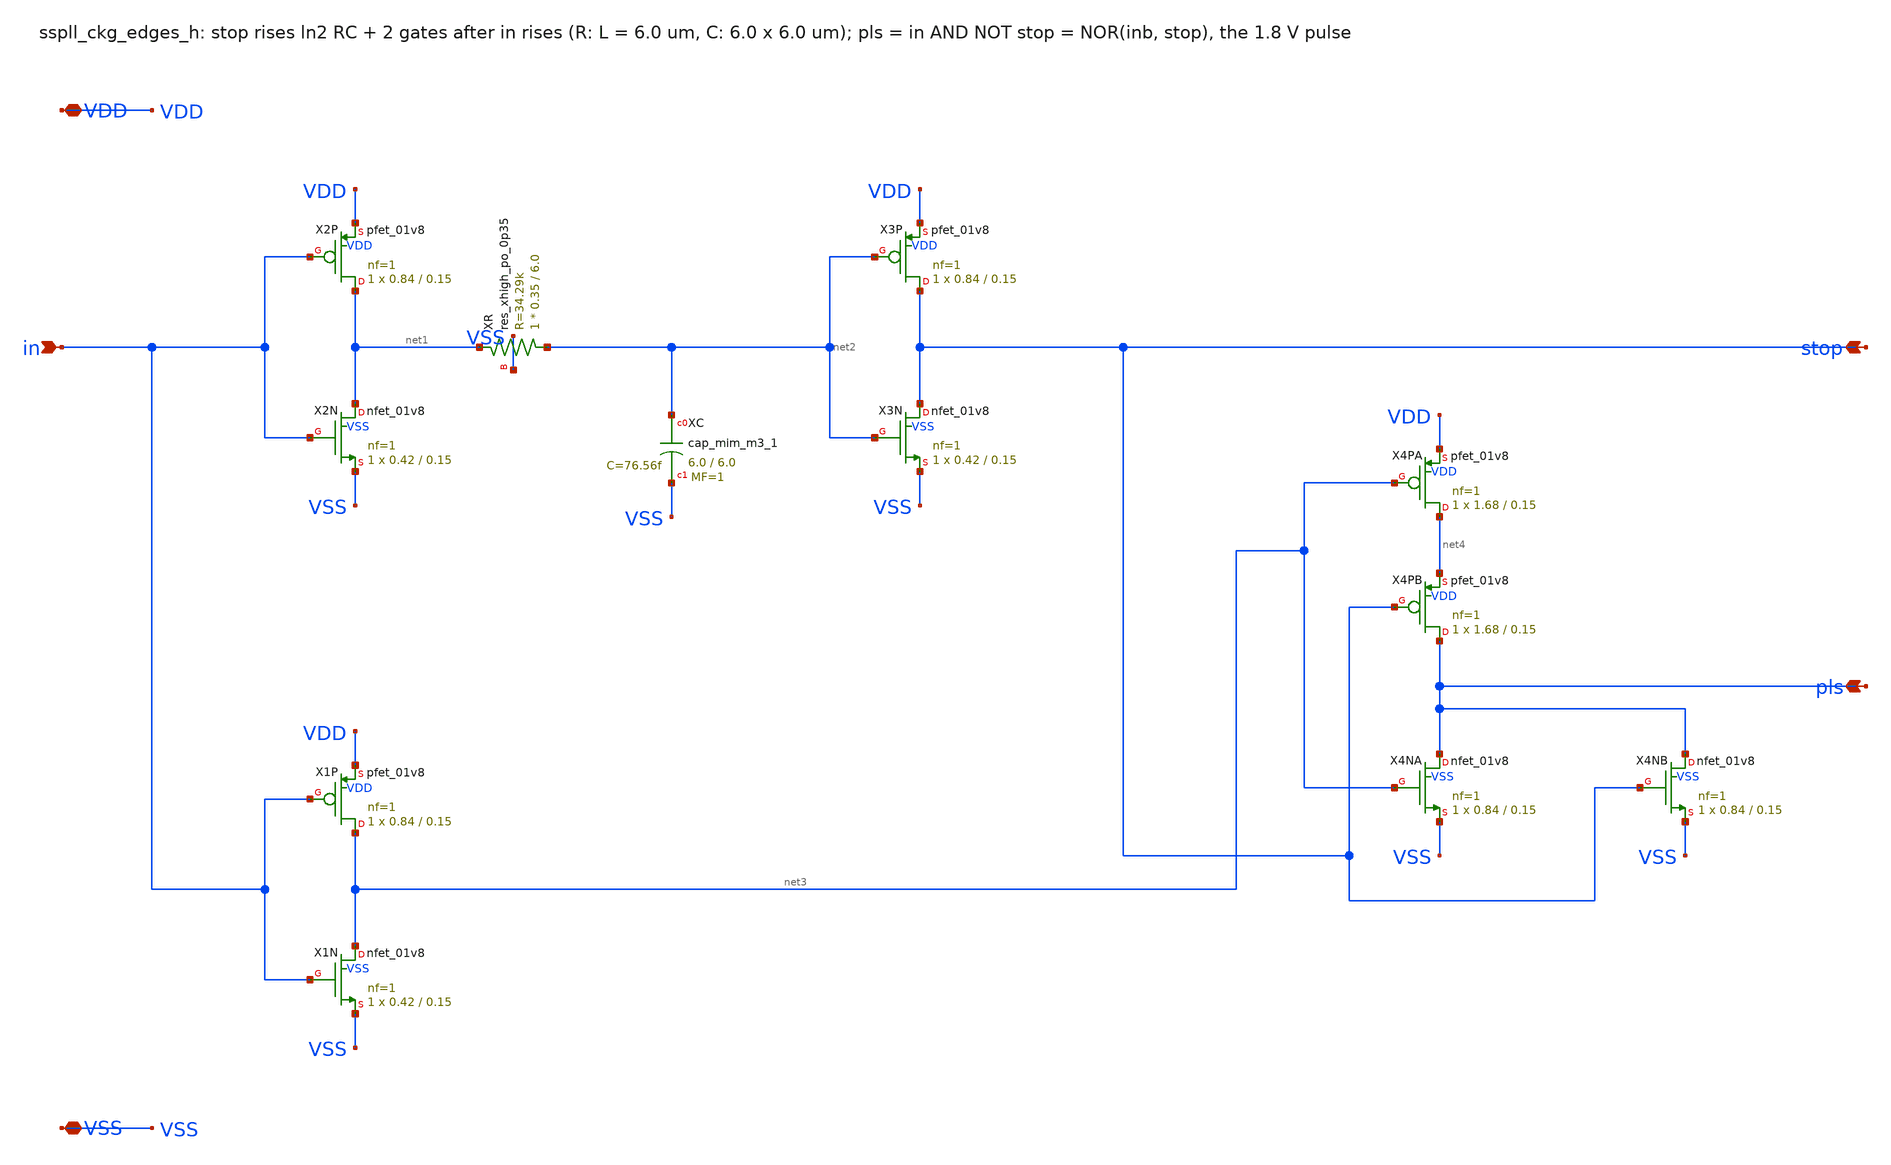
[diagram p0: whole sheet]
** sch_path: xschem/clkgen_hv/sspll_ckg_edges_h.sch
**.subckt sspll_ckg_edges_h in stop pls VDD VSS
*.ipin in
*.opin stop
*.opin pls
*.iopin VDD
*.iopin VSS
XX2P net1 in VDD VDD sky130_fd_pr__pfet_01v8 L=0.15 W=0.84 nf=1 ad='int((nf+1)/2) * W/nf * 0.29' as='int((nf+2)/2) * W/nf * 0.29'
+ pd='2*int((nf+1)/2) * (W/nf + 0.29)' ps='2*int((nf+2)/2) * (W/nf + 0.29)' nrd='0.29 / W' nrs='0.29 / W'
+ sa=0 sb=0 sd=0 mult=1 m=1
XX2N net1 in VSS VSS sky130_fd_pr__nfet_01v8 L=0.15 W=0.42 nf=1 ad='int((nf+1)/2) * W/nf * 0.29' as='int((nf+2)/2) * W/nf * 0.29'
+ pd='2*int((nf+1)/2) * (W/nf + 0.29)' ps='2*int((nf+2)/2) * (W/nf + 0.29)' nrd='0.29 / W' nrs='0.29 / W'
+ sa=0 sb=0 sd=0 mult=1 m=1
XXR net2 net1 VSS sky130_fd_pr__res_xhigh_po_0p35 L=6.0 mult=1 m=1
XXC net2 VSS sky130_fd_pr__cap_mim_m3_1 W=6.0 L=6.0 MF=1 m=1
XX3P stop net2 VDD VDD sky130_fd_pr__pfet_01v8 L=0.15 W=0.84 nf=1 ad='int((nf+1)/2) * W/nf * 0.29' as='int((nf+2)/2) * W/nf * 0.29'
+ pd='2*int((nf+1)/2) * (W/nf + 0.29)' ps='2*int((nf+2)/2) * (W/nf + 0.29)' nrd='0.29 / W' nrs='0.29 / W'
+ sa=0 sb=0 sd=0 mult=1 m=1
XX3N stop net2 VSS VSS sky130_fd_pr__nfet_01v8 L=0.15 W=0.42 nf=1 ad='int((nf+1)/2) * W/nf * 0.29' as='int((nf+2)/2) * W/nf * 0.29'
+ pd='2*int((nf+1)/2) * (W/nf + 0.29)' ps='2*int((nf+2)/2) * (W/nf + 0.29)' nrd='0.29 / W' nrs='0.29 / W'
+ sa=0 sb=0 sd=0 mult=1 m=1
XX1P net3 in VDD VDD sky130_fd_pr__pfet_01v8 L=0.15 W=0.84 nf=1 ad='int((nf+1)/2) * W/nf * 0.29' as='int((nf+2)/2) * W/nf * 0.29'
+ pd='2*int((nf+1)/2) * (W/nf + 0.29)' ps='2*int((nf+2)/2) * (W/nf + 0.29)' nrd='0.29 / W' nrs='0.29 / W'
+ sa=0 sb=0 sd=0 mult=1 m=1
XX1N net3 in VSS VSS sky130_fd_pr__nfet_01v8 L=0.15 W=0.42 nf=1 ad='int((nf+1)/2) * W/nf * 0.29' as='int((nf+2)/2) * W/nf * 0.29'
+ pd='2*int((nf+1)/2) * (W/nf + 0.29)' ps='2*int((nf+2)/2) * (W/nf + 0.29)' nrd='0.29 / W' nrs='0.29 / W'
+ sa=0 sb=0 sd=0 mult=1 m=1
XX4PA net4 net3 VDD VDD sky130_fd_pr__pfet_01v8 L=0.15 W=1.68 nf=1 ad='int((nf+1)/2) * W/nf * 0.29' as='int((nf+2)/2) * W/nf * 0.29'
+ pd='2*int((nf+1)/2) * (W/nf + 0.29)' ps='2*int((nf+2)/2) * (W/nf + 0.29)' nrd='0.29 / W' nrs='0.29 / W'
+ sa=0 sb=0 sd=0 mult=1 m=1
XX4PB pls stop net4 VDD sky130_fd_pr__pfet_01v8 L=0.15 W=1.68 nf=1 ad='int((nf+1)/2) * W/nf * 0.29' as='int((nf+2)/2) * W/nf * 0.29'
+ pd='2*int((nf+1)/2) * (W/nf + 0.29)' ps='2*int((nf+2)/2) * (W/nf + 0.29)' nrd='0.29 / W' nrs='0.29 / W'
+ sa=0 sb=0 sd=0 mult=1 m=1
XX4NA pls net3 VSS VSS sky130_fd_pr__nfet_01v8 L=0.15 W=0.84 nf=1 ad='int((nf+1)/2) * W/nf * 0.29' as='int((nf+2)/2) * W/nf * 0.29'
+ pd='2*int((nf+1)/2) * (W/nf + 0.29)' ps='2*int((nf+2)/2) * (W/nf + 0.29)' nrd='0.29 / W' nrs='0.29 / W'
+ sa=0 sb=0 sd=0 mult=1 m=1
XX4NB pls stop VSS VSS sky130_fd_pr__nfet_01v8 L=0.15 W=0.84 nf=1 ad='int((nf+1)/2) * W/nf * 0.29' as='int((nf+2)/2) * W/nf * 0.29'
+ pd='2*int((nf+1)/2) * (W/nf + 0.29)' ps='2*int((nf+2)/2) * (W/nf + 0.29)' nrd='0.29 / W' nrs='0.29 / W'
+ sa=0 sb=0 sd=0 mult=1 m=1
**.ends
.end
